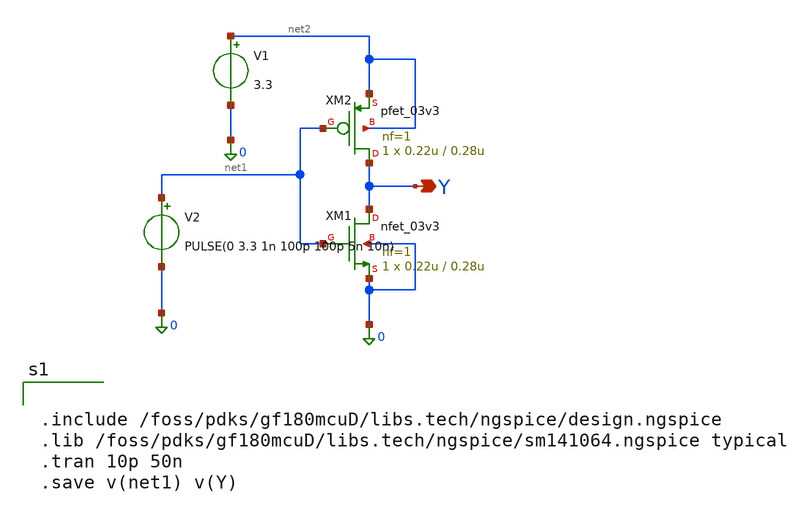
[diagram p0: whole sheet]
** sch_path: designs/libs/core_analog/lna/lna_core.sch
**.subckt lna_core Y
*.opin Y
XM1 Y net1 0 0 nfet_03v3 L=0.28u W=0.22u nf=1 ad='int((nf+1)/2) * W/nf * 0.18u' as='int((nf+2)/2) * W/nf * 0.18u'
+ pd='2*int((nf+1)/2) * (W/nf + 0.18u)' ps='2*int((nf+2)/2) * (W/nf + 0.18u)' nrd='0.18u / W' nrs='0.18u / W'
+ sa=0 sb=0 sd=0 m=1
XM2 Y net1 net2 net2 pfet_03v3 L=0.28u W=0.22u nf=1 ad='int((nf+1)/2) * W/nf * 0.18u' as='int((nf+2)/2) * W/nf * 0.18u'
+ pd='2*int((nf+1)/2) * (W/nf + 0.18u)' ps='2*int((nf+2)/2) * (W/nf + 0.18u)' nrd='0.18u / W' nrs='0.18u / W'
+ sa=0 sb=0 sd=0 m=1
V1 net2 0 3.3
V2 net1 0 PULSE(0 3.3 1n 100p 100p 5n 10n)
**** begin user architecture code


.include /foss/pdks/gf180mcuD/libs.tech/ngspice/design.ngspice
.lib /foss/pdks/gf180mcuD/libs.tech/ngspice/sm141064.ngspice typical
.tran 10p 50n
.save v(net1) v(Y)

**** end user architecture code
**.ends
.end
